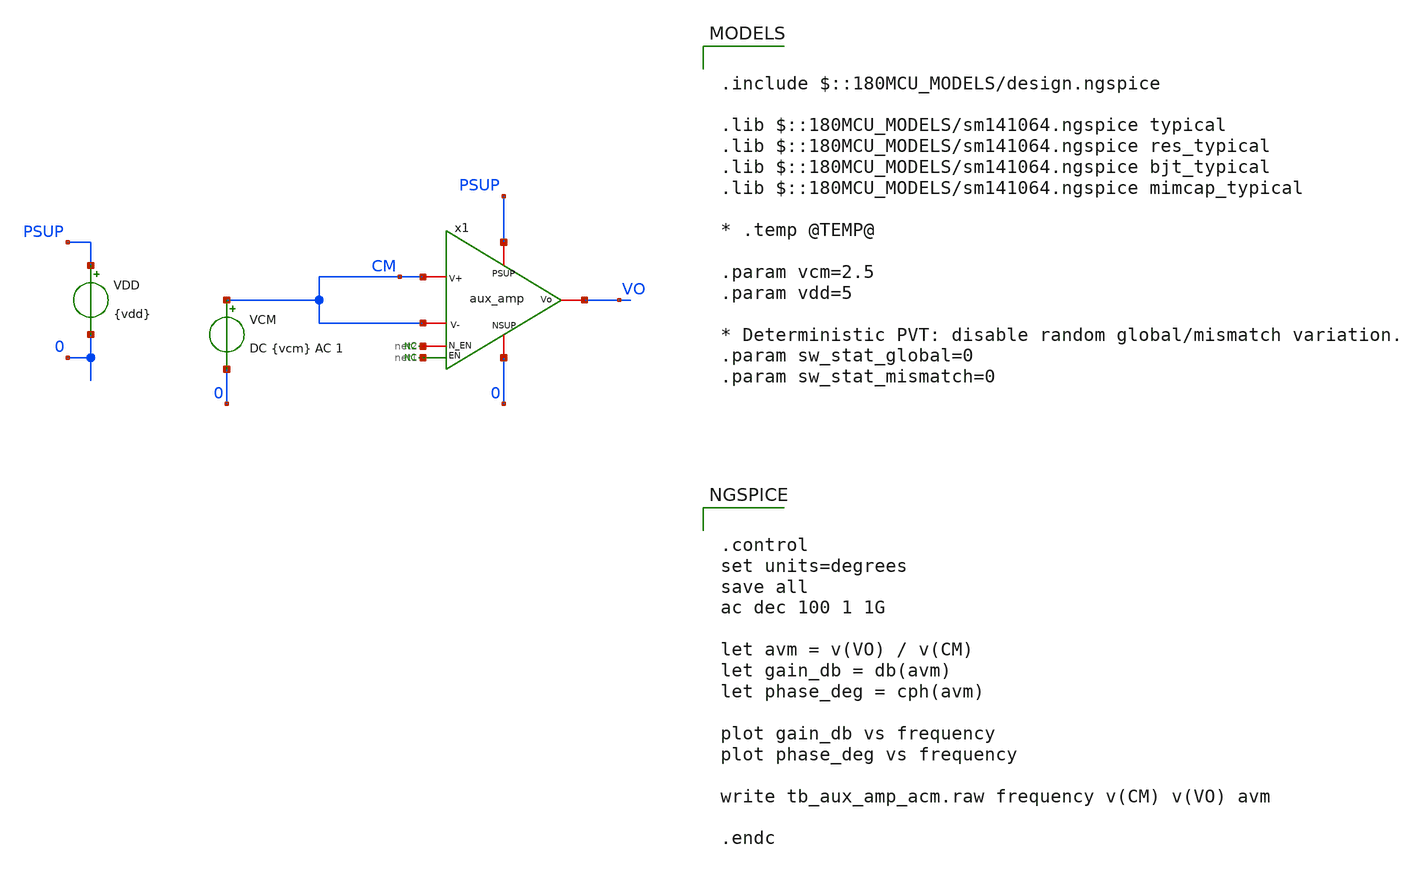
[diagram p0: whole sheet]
** sch_path: xschem/blocks/error_amp/tb_aux_amp_acm.sch
**.subckt tb_aux_amp_acm
VDD PSUP 0 {vdd}
VCM CM 0 DC {vcm} AC 1
* noconn #net1
* noconn #net2
x1 PSUP VO CM CM net2 0 net1 aux_amp
**** begin user architecture code

.include $::180MCU_MODELS/design.ngspice

.lib $::180MCU_MODELS/sm141064.ngspice typical
.lib $::180MCU_MODELS/sm141064.ngspice res_typical
.lib $::180MCU_MODELS/sm141064.ngspice bjt_typical
.lib $::180MCU_MODELS/sm141064.ngspice mimcap_typical

* .temp @TEMP@

.param vcm=2.5
.param vdd=5

* Deterministic PVT: disable random global/mismatch variation.
.param sw_stat_global=0
.param sw_stat_mismatch=0



.control
set units=degrees
save all
ac dec 100 1 1G

let avm = v(VO) / v(CM)
let gain_db = db(avm)
let phase_deg = cph(avm)

plot gain_db vs frequency
plot phase_deg vs frequency

write tb_aux_amp_acm.raw frequency v(CM) v(VO) avm

.endc


**** end user architecture code
**.ends

* expanding   symbol:  blocks/aux_amp/aux_amp.sym # of pins=7
** sym_path: xschem/lib/aux_amp.sym
** sch_path: xschem/lib/aux_amp.sch
.subckt aux_amp PSUP Vo V+ V- N_EN NSUP EN
*.ipin PSUP
*.ipin NSUP
*.ipin N_EN
*.ipin EN
*.ipin V+
*.ipin V-
*.opin Vo
XM1 Vo V- net2 net2 nfet_06v0 L=1.80u W=0.80u nf=1 ad='int((nf+1)/2) * W/nf * 0.18u' as='int((nf+2)/2) * W/nf * 0.18u'
+ pd='2*int((nf+1)/2) * (W/nf + 0.18u)' ps='2*int((nf+2)/2) * (W/nf + 0.18u)' nrd='0.18u / W' nrs='0.18u / W'
+ sa=0 sb=0 sd=0 m=1
XM2 net1 V+ net2 net2 nfet_06v0 L=1.80u W=0.80u nf=1 ad='int((nf+1)/2) * W/nf * 0.18u' as='int((nf+2)/2) * W/nf * 0.18u'
+ pd='2*int((nf+1)/2) * (W/nf + 0.18u)' ps='2*int((nf+2)/2) * (W/nf + 0.18u)' nrd='0.18u / W' nrs='0.18u / W'
+ sa=0 sb=0 sd=0 m=1
XM5 net1 net1 PSUP PSUP pfet_06v0 L=0.55u W=0.30u nf=1 ad='int((nf+1)/2) * W/nf * 0.18u' as='int((nf+2)/2) * W/nf * 0.18u'
+ pd='2*int((nf+1)/2) * (W/nf + 0.18u)' ps='2*int((nf+2)/2) * (W/nf + 0.18u)' nrd='0.18u / W' nrs='0.18u / W'
+ sa=0 sb=0 sd=0 m=1
XM6 Vo net1 PSUP PSUP pfet_06v0 L=0.55u W=0.30u nf=1 ad='int((nf+1)/2) * W/nf * 0.18u' as='int((nf+2)/2) * W/nf * 0.18u'
+ pd='2*int((nf+1)/2) * (W/nf + 0.18u)' ps='2*int((nf+2)/2) * (W/nf + 0.18u)' nrd='0.18u / W' nrs='0.18u / W'
+ sa=0 sb=0 sd=0 m=1
I0 net2 NSUP 5u
* noconn N_EN
* noconn EN
.ends

.end
